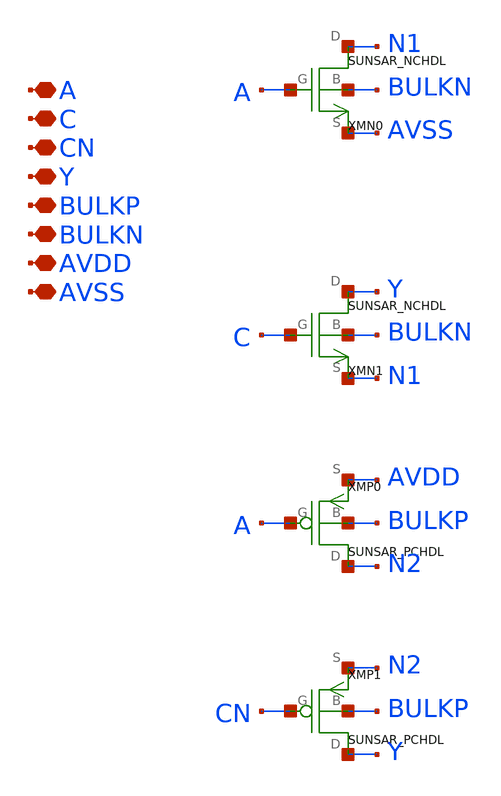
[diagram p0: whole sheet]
** sch_path: design/SUN_SAR9B_SKY130NM/SUNSAR_IVTRIX1_CV.sch
**.subckt SUNSAR_IVTRIX1_CV A C CN Y BULKP BULKN AVDD AVSS
*.iopin A
*.iopin C
*.iopin CN
*.iopin Y
*.iopin BULKP
*.iopin BULKN
*.iopin AVDD
*.iopin AVSS
XMN0 N1 A AVSS BULKN SUNSAR_NCHDL
XMN1 Y C N1 BULKN SUNSAR_NCHDL
XMP0 N2 A AVDD BULKP SUNSAR_PCHDL
XMP1 Y CN N2 BULKP SUNSAR_PCHDL
**.ends
.end
